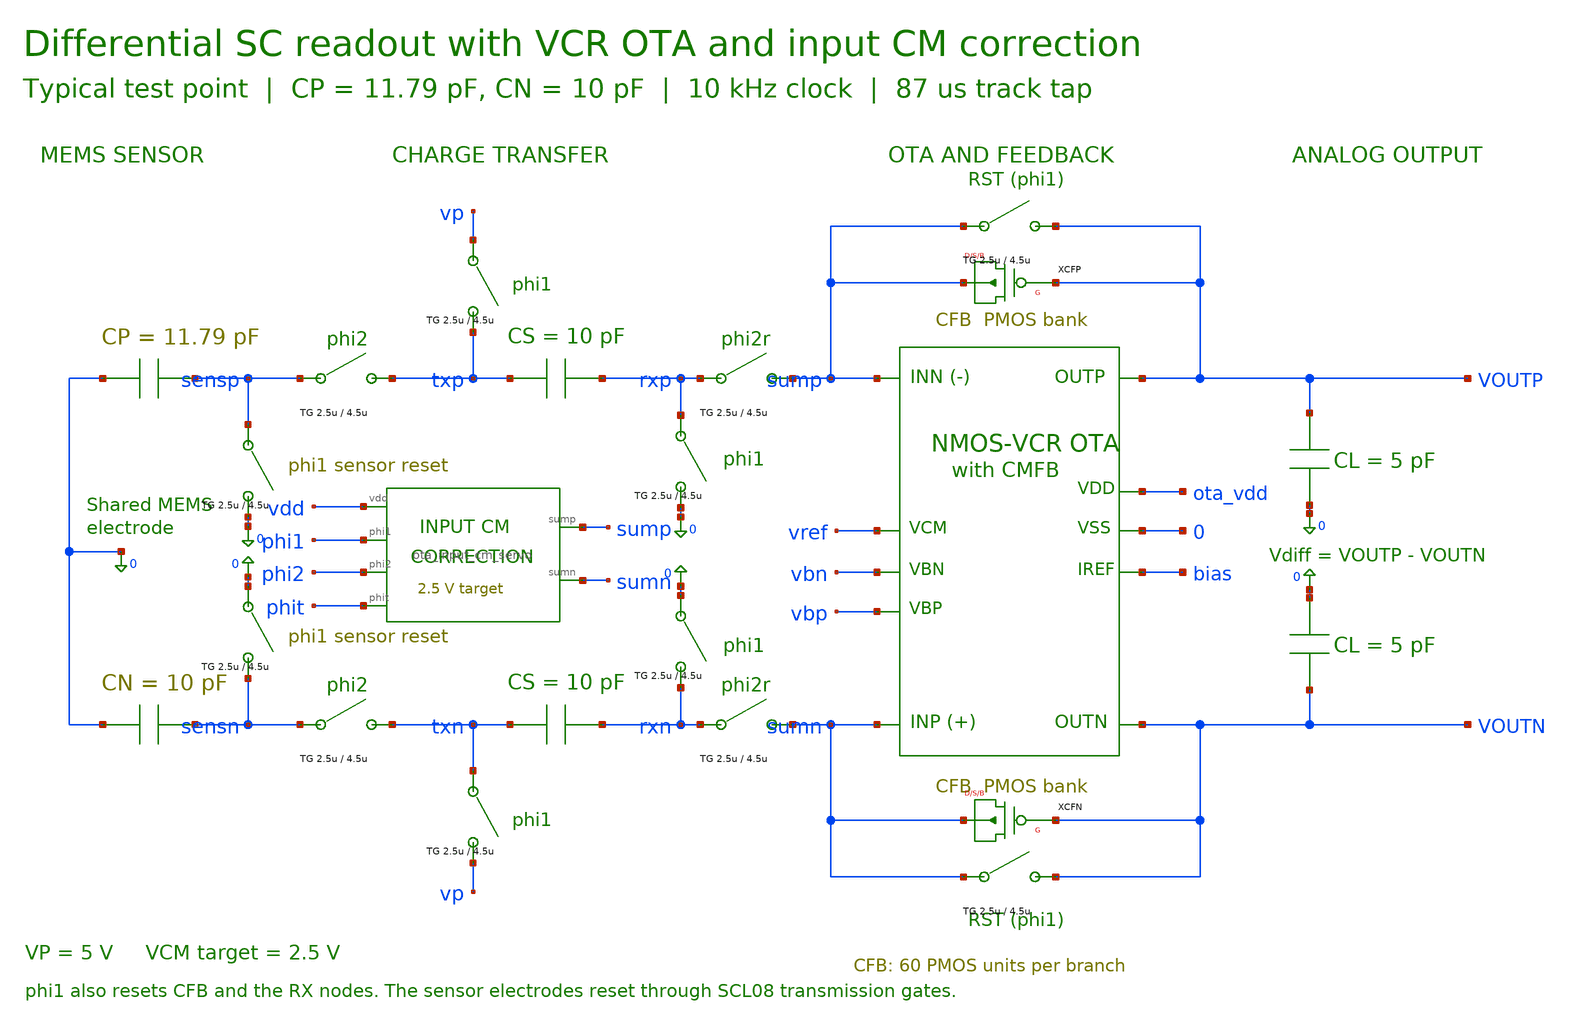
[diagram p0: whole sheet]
** sch_path: Mixed_Signal/Integrated_Design/schematic/sc_vcr_input_cm.sch
**.subckt sc_vcr_input_cm
XOTA sumn sump outp outn ota_vdd 0 bias vref vbn vbp ota_telescopic_cm2p5
CMEMP 0 sensp 11.79p
XSENSEP phi2 0 sensp txp vdd phi2b Transmission_v1_26
XSRESETP phi1 0 sensp 0 vdd phi1b Transmission_v1_26
XCHARGEP phi1 0 vp txp vdd phi1b Transmission_v1_26
CSP txp rxp 10p
XRRESETP phi1 0 rxp 0 vdd phi1b Transmission_v1_26
XXFERP phit 0 rxp sump vdd phitb Transmission_v1_26
XCFP sump outp sump sump P W=20u L=202.7u M=5 AD='( 20u ) * 4.5u' AS='( 20u ) * 4.5u' PD='2 * ( 20u ) + 9u'
+ PS='2 * ( 20u ) + 9u'
XFBRESETP phi1 0 sump outp vdd phi1b Transmission_v1_26
CLP outp 0 5p
CMEMN 0 sensn 10p
XSENSEN phi2 0 sensn txn vdd phi2b Transmission_v1_26
XSRESETN phi1 0 0 sensn vdd phi1b Transmission_v1_26
XCHARGEN phi1 0 txn vp vdd phi1b Transmission_v1_26
CSN txn rxn 10p
XRRESETN phi1 0 0 rxn vdd phi1b Transmission_v1_26
XXFERN phit 0 rxn sumn vdd phitb Transmission_v1_26
XCFN sumn outn sumn sumn P W=20u L=202.7u M=5 AD='( 20u ) * 4.5u' AS='( 20u ) * 4.5u' PD='2 * ( 20u ) + 9u'
+ PS='2 * ( 20u ) + 9u'
XFBRESETN phi1 0 sumn outn vdd phi1b Transmission_v1_26
CLN 0 outn 5p
XICM sump sumn vdd phi1 phi2 phit ota_input_cm_servo
**** begin user architecture code
.include /home/shreyas/Desktop/Sec_7/Integrated_Design/simulation/original_support.spice
**** end user architecture code
**.ends

* expanding   symbol:  /home/shreyas/Desktop/Sec_7/Integrated_Design/symbols/ota_input_cm_servo.sym
*+ # of pins=6
** sym_path: Mixed_Signal/Integrated_Design/symbols/ota_input_cm_servo.sym
** sch_path: Mixed_Signal/Integrated_Design/symbols/ota_input_cm_servo.sch
.subckt ota_input_cm_servo sump sumn vdd phi1 phi2 phit
*.iopin vdd
*.iopin phit
*.iopin phi1
*.iopin phi2
*.iopin sump
*.iopin sumn
BICMERR 0 cm_acc I = 1m*v(cm_sample)*(2.5-(v(sump)+v(sumn))/2)
CICMINT cm_acc 0 1n m=1
RICMINT cm_acc 0 1e13 m=1
VICMSAMPLE cm_sample 0 PULSE(0 1 84u 10n 10n 2u 100u)
BICMCTRL cm_ctrl 0 V = max(0,min(v(vdd),2.5+v(cm_acc)))
XSICMHOLD cm_ctrl cm_hold phi1 vdd user_tg_control
CICMHOLD cm_hold 0 20p m=1
RICMHOLD cm_hold cm_init 1e13 m=1
VICMINIT cm_init 0 2.5
XSICMEDGE1 vdd cm_edge1 phit vdd user_tg_control
XSICMRST1 0 cm_edge1 phi1 vdd user_tg_control
CICMEDGE1 cm_edge1 0 10p m=1
XSICMEDGE2 vdd cm_edge2 phi2 vdd user_tg_control
XSICMRST2 0 cm_edge2 phi1 vdd user_tg_control
CICMEDGE2 cm_edge2 0 10p m=1
BICMDRIVE cm_x 0 V = ((.68*v(cm_edge1)+.32*v(cm_edge2))/max(.1,v(vdd)))*v(cm_hold)
MCORRp sump cm_x sump sump P W=20u L=10u M=40 AD=90p AS=90p PD=49u PS=49u
MCORRn sumn cm_x sumn sumn P W=20u L=10u M=40 AD=90p AS=90p PD=49u PS=49u
**** begin user architecture code
.model icm_hold SW(Ron=10 Roff=1e14 Vt=2 Vh=.1)
.model icm_edge_set SW(Ron=3000 Roff=1e13 Vt=1 Vh=.05)
.model icm_edge_reset SW(Ron=100k Roff=1e13 Vt=2 Vh=.1)
**** end user architecture code
.ends

.end
